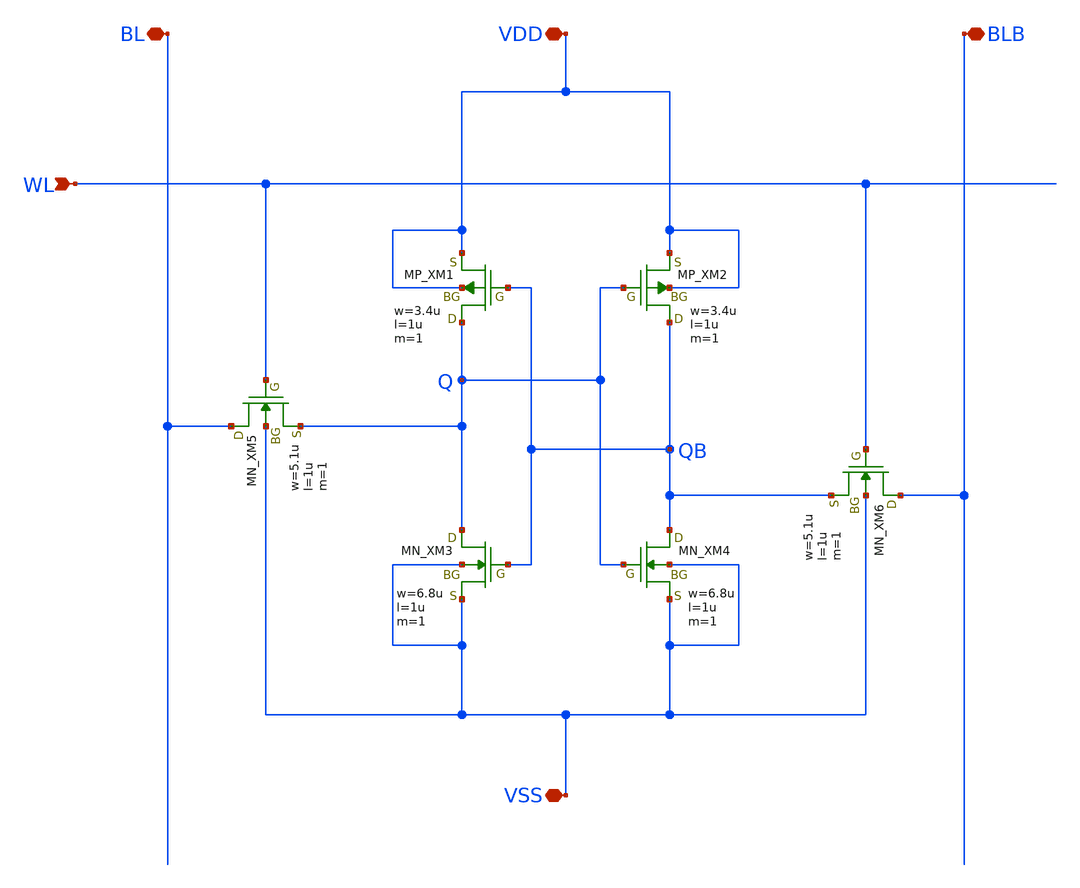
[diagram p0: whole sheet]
** sch_path: cell/snm/sram6t_tr10.sch
**.subckt sram6t_tr10 BL BLB WL VDD VSS
*.iopin BL
*.iopin BLB
*.ipin WL
*.iopin VDD
*.iopin VSS
XXM1 Q QB VDD VDD PMOS w=3.4u l=1u nrd=0 nrs=0 m=1
XXM2 QB Q VDD VDD PMOS w=3.4u l=1u nrd=0 nrs=0 m=1
XXM4 QB Q VSS VSS NMOS w=6.8u l=1u nrd=0 nrs=0 m=1
XXM3 Q QB VSS VSS NMOS w=6.8u l=1u nrd=0 nrs=0 m=1
XXM5 BL WL Q VSS NMOS w=5.1u l=1u nrd=0 nrs=0 m=1
XXM6 BLB WL QB VSS NMOS w=5.1u l=1u nrd=0 nrs=0 m=1
**.ends
.end
